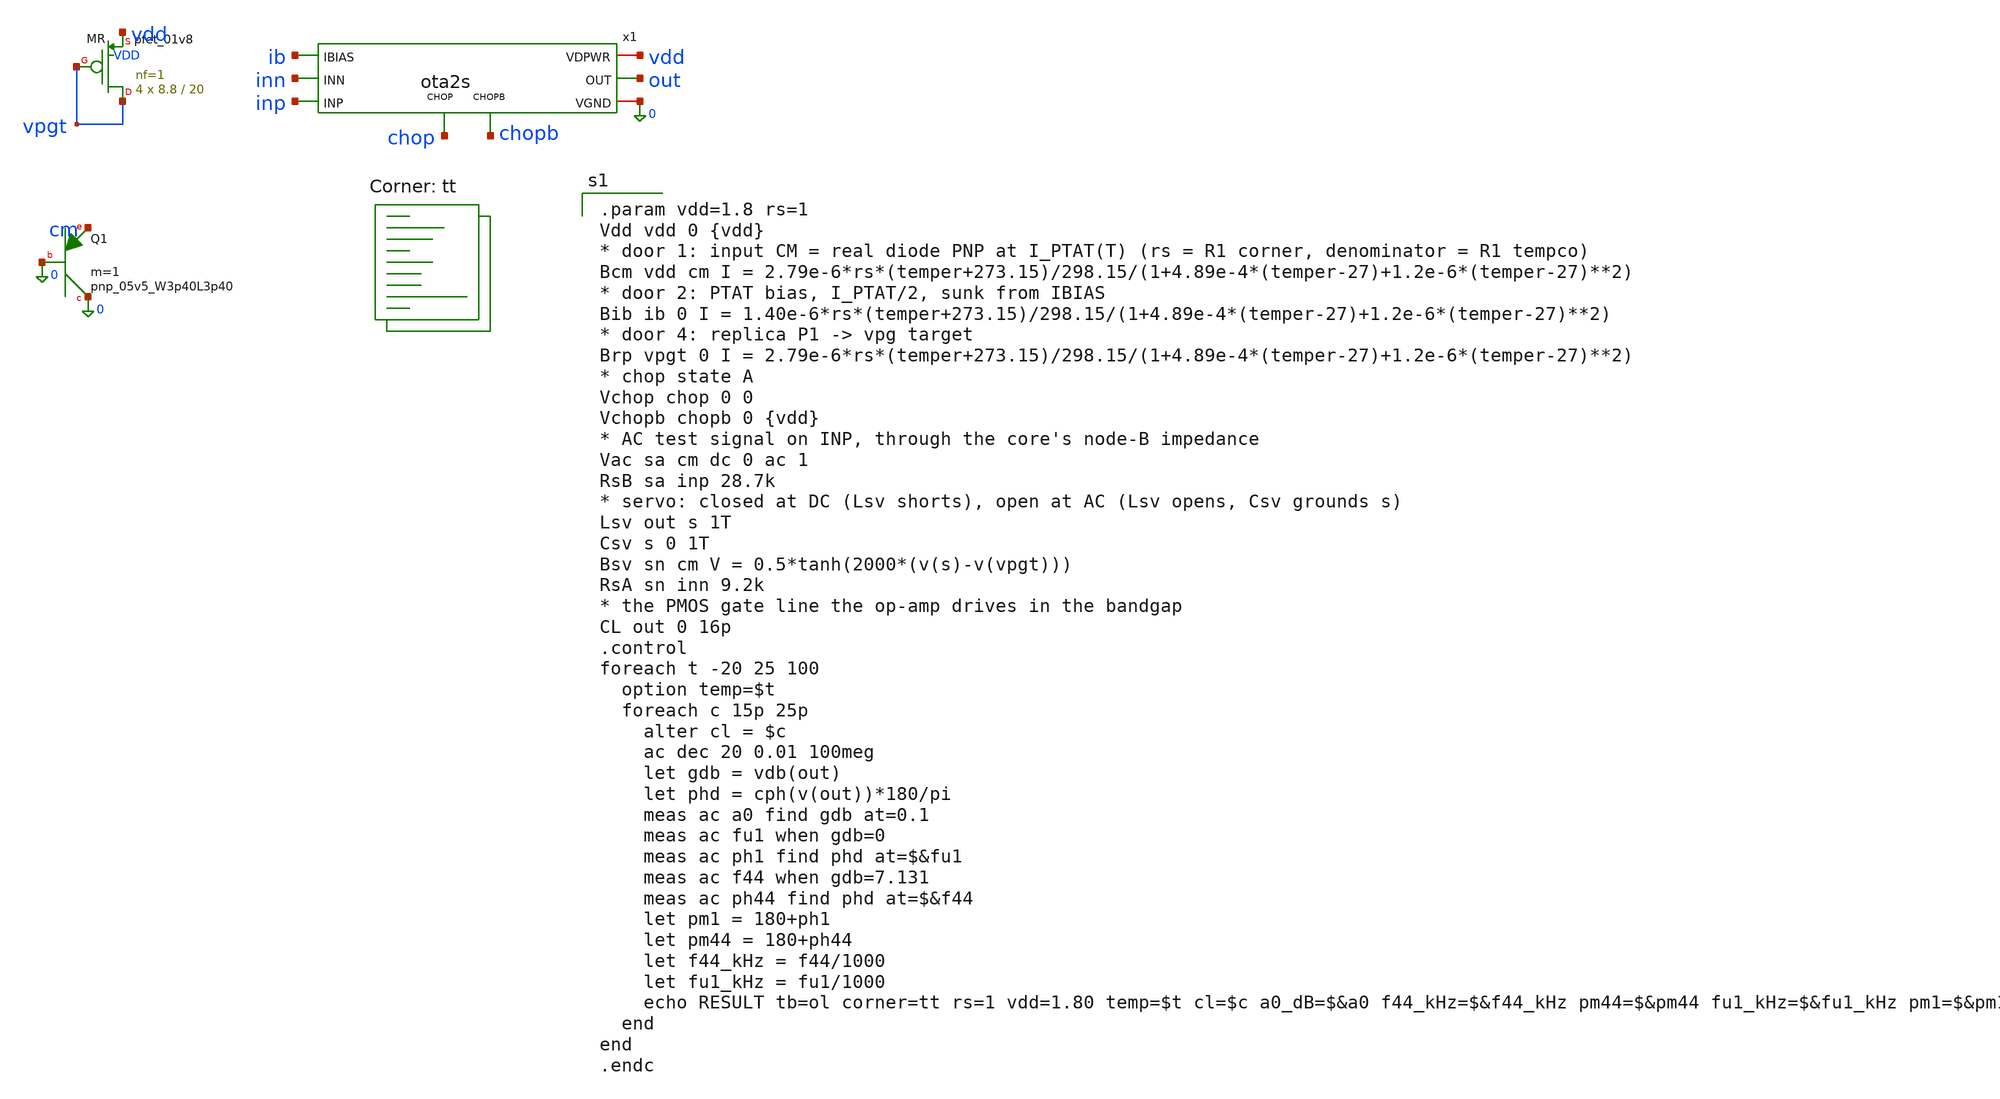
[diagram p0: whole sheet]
** sch_path: xschem/tb_m3_ol.sch
**.subckt tb_m3_ol
x1 inp inn out vdd 0 ib chop chopb ota2s
XMR vpgt vpgt vdd VDD sky130_fd_pr__pfet_01v8 L=20 W=8.8 nf=1 ad='int((1 + 1)/2) * 8.8 / 1 * 0.29' as='int((1 + 2)/2) * 8.8 / 1 * 0.29'
+ pd='2*int((1 + 1)/2) * (8.8 / 1 + 0.29)' ps='2*int((1 + 2)/2) * (8.8 / 1 + 0.29)' nrd='0.29 / 8.8 ' nrs='0.29 / 8.8 '
+ sa=0 sb=0 sd=0 mult=4 m=4
XQ1 0 0 cm sky130_fd_pr__pnp_05v5_W3p40L3p40 m=1
**** begin user architecture code
.lib $::SKYWATER_MODELS/sky130.lib.spice tt

.param vdd=1.8 rs=1
Vdd vdd 0 {vdd}
* door 1: input CM = real diode PNP at I_PTAT(T) (rs = R1 corner, denominator = R1 tempco)
Bcm vdd cm I = 2.79e-6*rs*(temper+273.15)/298.15/(1+4.89e-4*(temper-27)+1.2e-6*(temper-27)**2)
* door 2: PTAT bias, I_PTAT/2, sunk from IBIAS
Bib ib 0 I = 1.40e-6*rs*(temper+273.15)/298.15/(1+4.89e-4*(temper-27)+1.2e-6*(temper-27)**2)
* door 4: replica P1 -> vpg target
Brp vpgt 0 I = 2.79e-6*rs*(temper+273.15)/298.15/(1+4.89e-4*(temper-27)+1.2e-6*(temper-27)**2)
* chop state A
Vchop chop 0 0
Vchopb chopb 0 {vdd}
* AC test signal on INP, through the core's node-B impedance
Vac sa cm dc 0 ac 1
RsB sa inp 28.7k
* servo: closed at DC (Lsv shorts), open at AC (Lsv opens, Csv grounds s)
Lsv out s 1T
Csv s 0 1T
Bsv sn cm V = 0.5*tanh(2000*(v(s)-v(vpgt)))
RsA sn inn 9.2k
* the PMOS gate line the op-amp drives in the bandgap
CL out 0 16p
.control
foreach t -20 25 100
  option temp=$t
  foreach c 15p 25p
    alter cl = $c
    ac dec 20 0.01 100meg
    let gdb = vdb(out)
    let phd = cph(v(out))*180/pi
    meas ac a0 find gdb at=0.1
    meas ac fu1 when gdb=0
    meas ac ph1 find phd at=$&fu1
    meas ac f44 when gdb=7.131
    meas ac ph44 find phd at=$&f44
    let pm1 = 180+ph1
    let pm44 = 180+ph44
    let f44_kHz = f44/1000
    let fu1_kHz = fu1/1000
    echo RESULT tb=ol corner=tt rs=1 vdd=1.80 temp=$t cl=$c a0_dB=$&a0 f44_kHz=$&f44_kHz pm44=$&pm44 fu1_kHz=$&fu1_kHz pm1=$&pm1
  end
end
.endc

**** end user architecture code
**.ends

* expanding   symbol:  ota2s.sym # of pins=8
** sym_path: xschem/ota2s.sym
** sch_path: xschem/ota2s.sch
.subckt ota2s INP INN OUT VDPWR VGND IBIAS CHOP CHOPB
*.ipin INN
*.ipin INP
*.ipin IBIAS
*.opin OUT
*.iopin VDPWR
*.iopin VGND
*.ipin CHOPB
*.ipin CHOP
XMREF IBIAS IBIAS VDPWR VDPWR sky130_fd_pr__pfet_01v8 L=4 W=20 nf=1 ad='int((1 + 1)/2) * 20 / 1 * 0.29' as='int((1
+ + 2)/2) * 20 / 1 * 0.29' pd='2*int((1 + 1)/2) * (20 / 1 + 0.29)' ps='2*int((1 + 2)/2) * (20 / 1 + 0.29)' nrd='0.29
+ / 20 ' nrs='0.29 / 20 ' sa=0 sb=0 sd=0 mult=1 m=1
XMTAIL tail IBIAS VDPWR VDPWR sky130_fd_pr__pfet_01v8 L=4 W=20 nf=1 ad='int((1 + 1)/2) * 20 / 1 * 0.29' as='int((1
+ + 2)/2) * 20 / 1 * 0.29' pd='2*int((1 + 1)/2) * (20 / 1 + 0.29)' ps='2*int((1 + 2)/2) * (20 / 1 + 0.29)' nrd='0.29
+ / 20 ' nrs='0.29 / 20 ' sa=0 sb=0 sd=0 mult=2 m=2
XMP1 d1 INN tail VDPWR sky130_fd_pr__pfet_01v8_lvt L=6 W=25 nf=1 ad='int((1 + 1)/2) * 25 / 1 * 0.29' as='int((1
+ + 2)/2) * 25 / 1 * 0.29' pd='2*int((1 + 1)/2) * (25 / 1 + 0.29)' ps='2*int((1 + 2)/2) * (25 / 1 + 0.29)' nrd='0.29
+ / 25 ' nrs='0.29 / 25 ' sa=0 sb=0 sd=0 mult=24 m=24
XMP2 x1 INP tail VDPWR sky130_fd_pr__pfet_01v8_lvt L=6 W=25 nf=1 ad='int((1 + 1)/2) * 25 / 1 * 0.29' as='int((1
+ + 2)/2) * 25 / 1 * 0.29' pd='2*int((1 + 1)/2) * (25 / 1 + 0.29)' ps='2*int((1 + 2)/2) * (25 / 1 + 0.29)' nrd='0.29
+ / 25 ' nrs='0.29 / 25 ' sa=0 sb=0 sd=0 mult=24 m=24
XMN1 d1 g12 VGND VGND sky130_fd_pr__nfet_01v8 L=20 W=6 nf=1 ad='int((1 + 1)/2) * 6 / 1 * 0.29' as='int((1
+ + 2)/2) * 6 / 1 * 0.29' pd='2*int((1 + 1)/2) * (6 / 1 + 0.29)' ps='2*int((1 + 2)/2) * (6 / 1 + 0.29)' nrd='0.29
+ / 6 ' nrs='0.29 / 6 ' sa=0 sb=0 sd=0 mult=2 m=2
XMN2 x1 g12 VGND VGND sky130_fd_pr__nfet_01v8 L=20 W=6 nf=1 ad='int((1 + 1)/2) * 6 / 1 * 0.29' as='int((1
+ + 2)/2) * 6 / 1 * 0.29' pd='2*int((1 + 1)/2) * (6 / 1 + 0.29)' ps='2*int((1 + 2)/2) * (6 / 1 + 0.29)' nrd='0.29
+ / 6 ' nrs='0.29 / 6 ' sa=0 sb=0 sd=0 mult=2 m=2
XMP3 OUT IBIAS VDPWR VDPWR sky130_fd_pr__pfet_01v8 L=4 W=20 nf=1 ad='int((1 + 1)/2) * 20 / 1 * 0.29' as='int((1
+ + 2)/2) * 20 / 1 * 0.29' pd='2*int((1 + 1)/2) * (20 / 1 + 0.29)' ps='2*int((1 + 2)/2) * (20 / 1 + 0.29)' nrd='0.29
+ / 20 ' nrs='0.29 / 20 ' sa=0 sb=0 sd=0 mult=6 m=6
XMN3 OUT g3 VGND VGND sky130_fd_pr__nfet_01v8 L=1 W=7 nf=1 ad='int((1 + 1)/2) * 7 / 1 * 0.29' as='int((1
+ + 2)/2) * 7 / 1 * 0.29' pd='2*int((1 + 1)/2) * (7 / 1 + 0.29)' ps='2*int((1 + 2)/2) * (7 / 1 + 0.29)' nrd='0.29
+ / 7 ' nrs='0.29 / 7 ' sa=0 sb=0 sd=0 mult=1 m=1
XRZ1 net1 g3 VGND sky130_fd_pr__res_high_po_1p41 L=20 mult=1 m=1
XRZ2 net2 net1 VGND sky130_fd_pr__res_high_po_1p41 L=20 mult=1 m=1
XRZ3 net3 net2 VGND sky130_fd_pr__res_high_po_1p41 L=20 mult=1 m=1
XRZ4 net4 net3 VGND sky130_fd_pr__res_high_po_1p41 L=20 mult=1 m=1
XRZ5 net5 net4 VGND sky130_fd_pr__res_high_po_1p41 L=20 mult=1 m=1
XRZ6 cz net5 VGND sky130_fd_pr__res_high_po_1p41 L=20 mult=1 m=1
XCC cz OUT sky130_fd_pr__cap_mim_m3_1 W=25 L=25 MF=8 m=8
XDP tail VDPWR tail VDPWR sky130_fd_pr__pfet_01v8_lvt L=6 W=25 nf=1 ad='int((1 + 1)/2) * 25 / 1 * 0.29' as='int((1
+ + 2)/2) * 25 / 1 * 0.29' pd='2*int((1 + 1)/2) * (25 / 1 + 0.29)' ps='2*int((1 + 2)/2) * (25 / 1 + 0.29)' nrd='0.29
+ / 25 ' nrs='0.29 / 25 ' sa=0 sb=0 sd=0 mult=8 m=8
XDNA d1 VGND VGND VGND sky130_fd_pr__nfet_01v8 L=20 W=6 nf=1 ad='int((1 + 1)/2) * 6 / 1 * 0.29' as='int((1
+ + 2)/2) * 6 / 1 * 0.29' pd='2*int((1 + 1)/2) * (6 / 1 + 0.29)' ps='2*int((1 + 2)/2) * (6 / 1 + 0.29)' nrd='0.29
+ / 6 ' nrs='0.29 / 6 ' sa=0 sb=0 sd=0 mult=2 m=2
XDNB x1 VGND VGND VGND sky130_fd_pr__nfet_01v8 L=20 W=6 nf=1 ad='int((1 + 1)/2) * 6 / 1 * 0.29' as='int((1
+ + 2)/2) * 6 / 1 * 0.29' pd='2*int((1 + 1)/2) * (6 / 1 + 0.29)' ps='2*int((1 + 2)/2) * (6 / 1 + 0.29)' nrd='0.29
+ / 6 ' nrs='0.29 / 6 ' sa=0 sb=0 sd=0 mult=2 m=2
XDB VDPWR VDPWR VDPWR VDPWR sky130_fd_pr__pfet_01v8 L=4 W=20 nf=1 ad='int((1 + 1)/2) * 20 / 1 * 0.29' as='int((1
+ + 2)/2) * 20 / 1 * 0.29' pd='2*int((1 + 1)/2) * (20 / 1 + 0.29)' ps='2*int((1 + 2)/2) * (20 / 1 + 0.29)' nrd='0.29
+ / 20 ' nrs='0.29 / 20 ' sa=0 sb=0 sd=0 mult=2 m=2
XRD1 VGND VGND VGND sky130_fd_pr__res_high_po_1p41 L=20 mult=1 m=1
XRD2 VGND VGND VGND sky130_fd_pr__res_high_po_1p41 L=20 mult=1 m=1
XSD1 d1 CHOPB g12 VGND sky130_fd_pr__nfet_01v8 L=0.5 W=6 nf=1 ad='int((1 + 1)/2) * 6 / 1 * 0.29' as='int((1
+ + 2)/2) * 6 / 1 * 0.29' pd='2*int((1 + 1)/2) * (6 / 1 + 0.29)' ps='2*int((1 + 2)/2) * (6 / 1 + 0.29)' nrd='0.29
+ / 6 ' nrs='0.29 / 6 ' sa=0 sb=0 sd=0 mult=1 m=1
XSD2 x1 CHOP g12 VGND sky130_fd_pr__nfet_01v8 L=0.5 W=6 nf=1 ad='int((1 + 1)/2) * 6 / 1 * 0.29' as='int((1
+ + 2)/2) * 6 / 1 * 0.29' pd='2*int((1 + 1)/2) * (6 / 1 + 0.29)' ps='2*int((1 + 2)/2) * (6 / 1 + 0.29)' nrd='0.29
+ / 6 ' nrs='0.29 / 6 ' sa=0 sb=0 sd=0 mult=1 m=1
XSG2 g3 CHOP d1 VGND sky130_fd_pr__nfet_01v8 L=0.5 W=6 nf=1 ad='int((1 + 1)/2) * 6 / 1 * 0.29' as='int((1
+ + 2)/2) * 6 / 1 * 0.29' pd='2*int((1 + 1)/2) * (6 / 1 + 0.29)' ps='2*int((1 + 2)/2) * (6 / 1 + 0.29)' nrd='0.29
+ / 6 ' nrs='0.29 / 6 ' sa=0 sb=0 sd=0 mult=1 m=1
XSG1 x1 CHOPB g3 VGND sky130_fd_pr__nfet_01v8 L=0.5 W=6 nf=1 ad='int((1 + 1)/2) * 6 / 1 * 0.29' as='int((1
+ + 2)/2) * 6 / 1 * 0.29' pd='2*int((1 + 1)/2) * (6 / 1 + 0.29)' ps='2*int((1 + 2)/2) * (6 / 1 + 0.29)' nrd='0.29
+ / 6 ' nrs='0.29 / 6 ' sa=0 sb=0 sd=0 mult=1 m=1
.ends

.end
